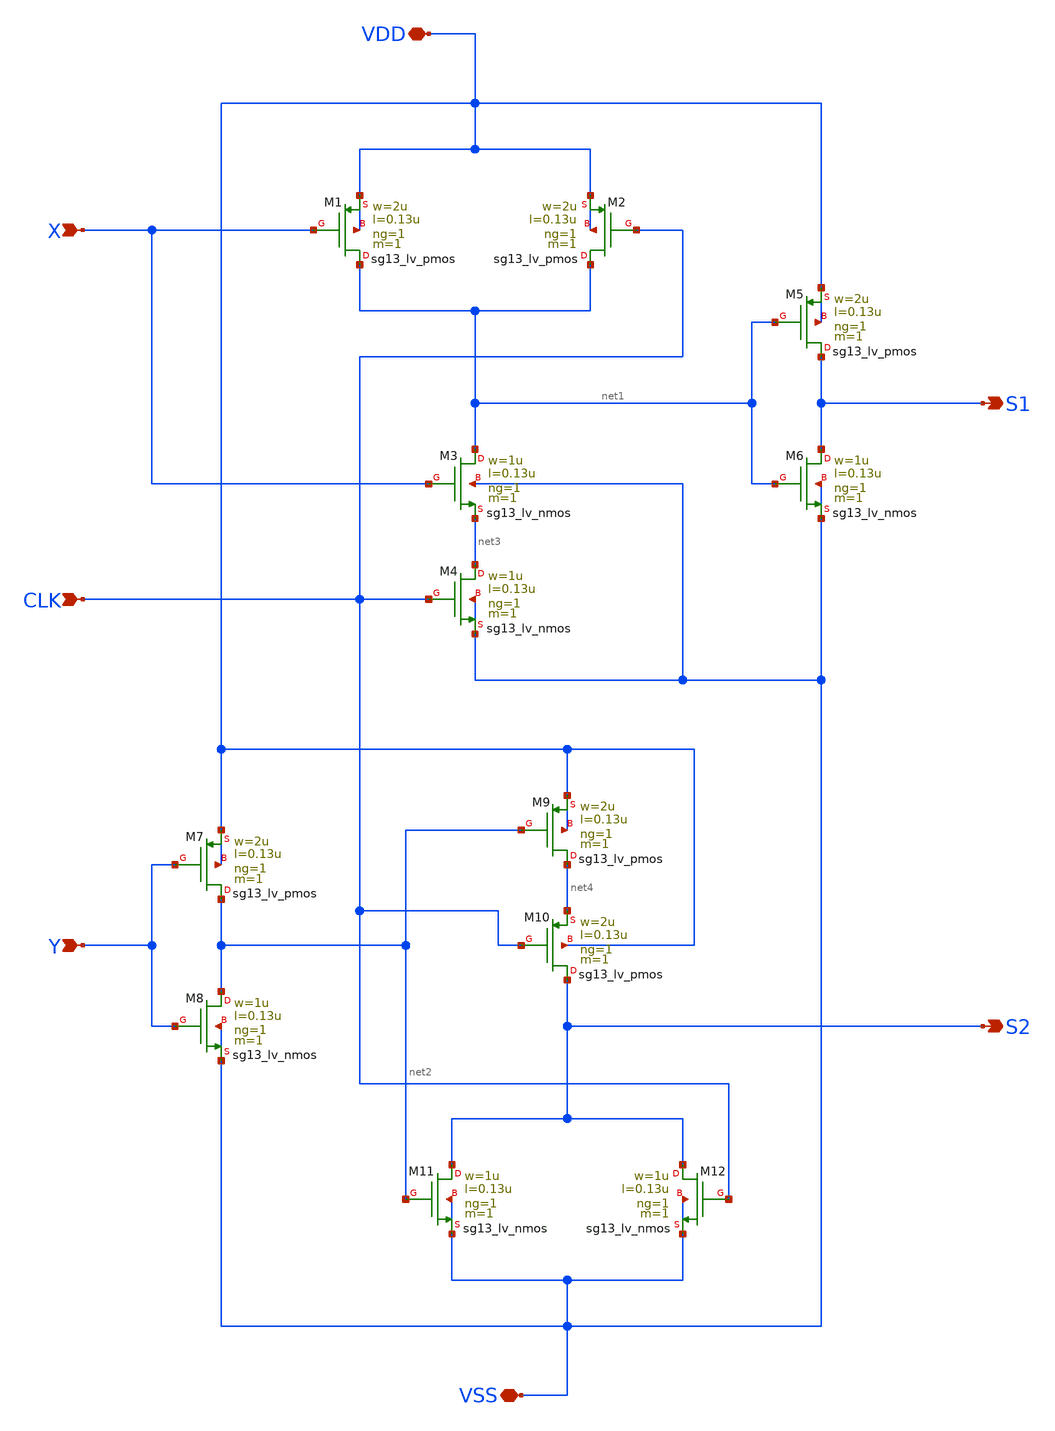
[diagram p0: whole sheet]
** sch_path: SSDOR_1.2V_v4/components/logic_controller/logic_controller.sch
**.subckt logic_controller X CLK Y S1 S2 VSS VDD
*.ipin X
*.ipin CLK
*.ipin Y
*.opin S1
*.opin S2
*.iopin VSS
*.iopin VDD
XM1 net1 X VDD VDD sg13_lv_pmos w=2u l=0.13u ng=1 m=1 mm_ok=1
XM2 net1 CLK VDD VDD sg13_lv_pmos w=2u l=0.13u ng=1 m=1 mm_ok=1
XM3 net1 X net3 VSS sg13_lv_nmos w=1u l=0.13u ng=1 m=1 mm_ok=1
XM4 net3 CLK VSS VSS sg13_lv_nmos w=1u l=0.13u ng=1 m=1 mm_ok=1
XM5 S1 net1 VDD VDD sg13_lv_pmos w=2u l=0.13u ng=1 m=1 mm_ok=1
XM6 S1 net1 VSS VSS sg13_lv_nmos w=1u l=0.13u ng=1 m=1 mm_ok=1
XM7 net2 Y VDD VDD sg13_lv_pmos w=2u l=0.13u ng=1 m=1 mm_ok=1
XM8 net2 Y VSS VSS sg13_lv_nmos w=1u l=0.13u ng=1 m=1 mm_ok=1
XM9 net4 net2 VDD VDD sg13_lv_pmos w=2u l=0.13u ng=1 m=1 mm_ok=1
XM10 S2 CLK net4 VDD sg13_lv_pmos w=2u l=0.13u ng=1 m=1 mm_ok=1
XM11 S2 net2 VSS VSS sg13_lv_nmos w=1u l=0.13u ng=1 m=1 mm_ok=1
XM12 S2 CLK VSS VSS sg13_lv_nmos w=1u l=0.13u ng=1 m=1 mm_ok=1
**.ends
.end
